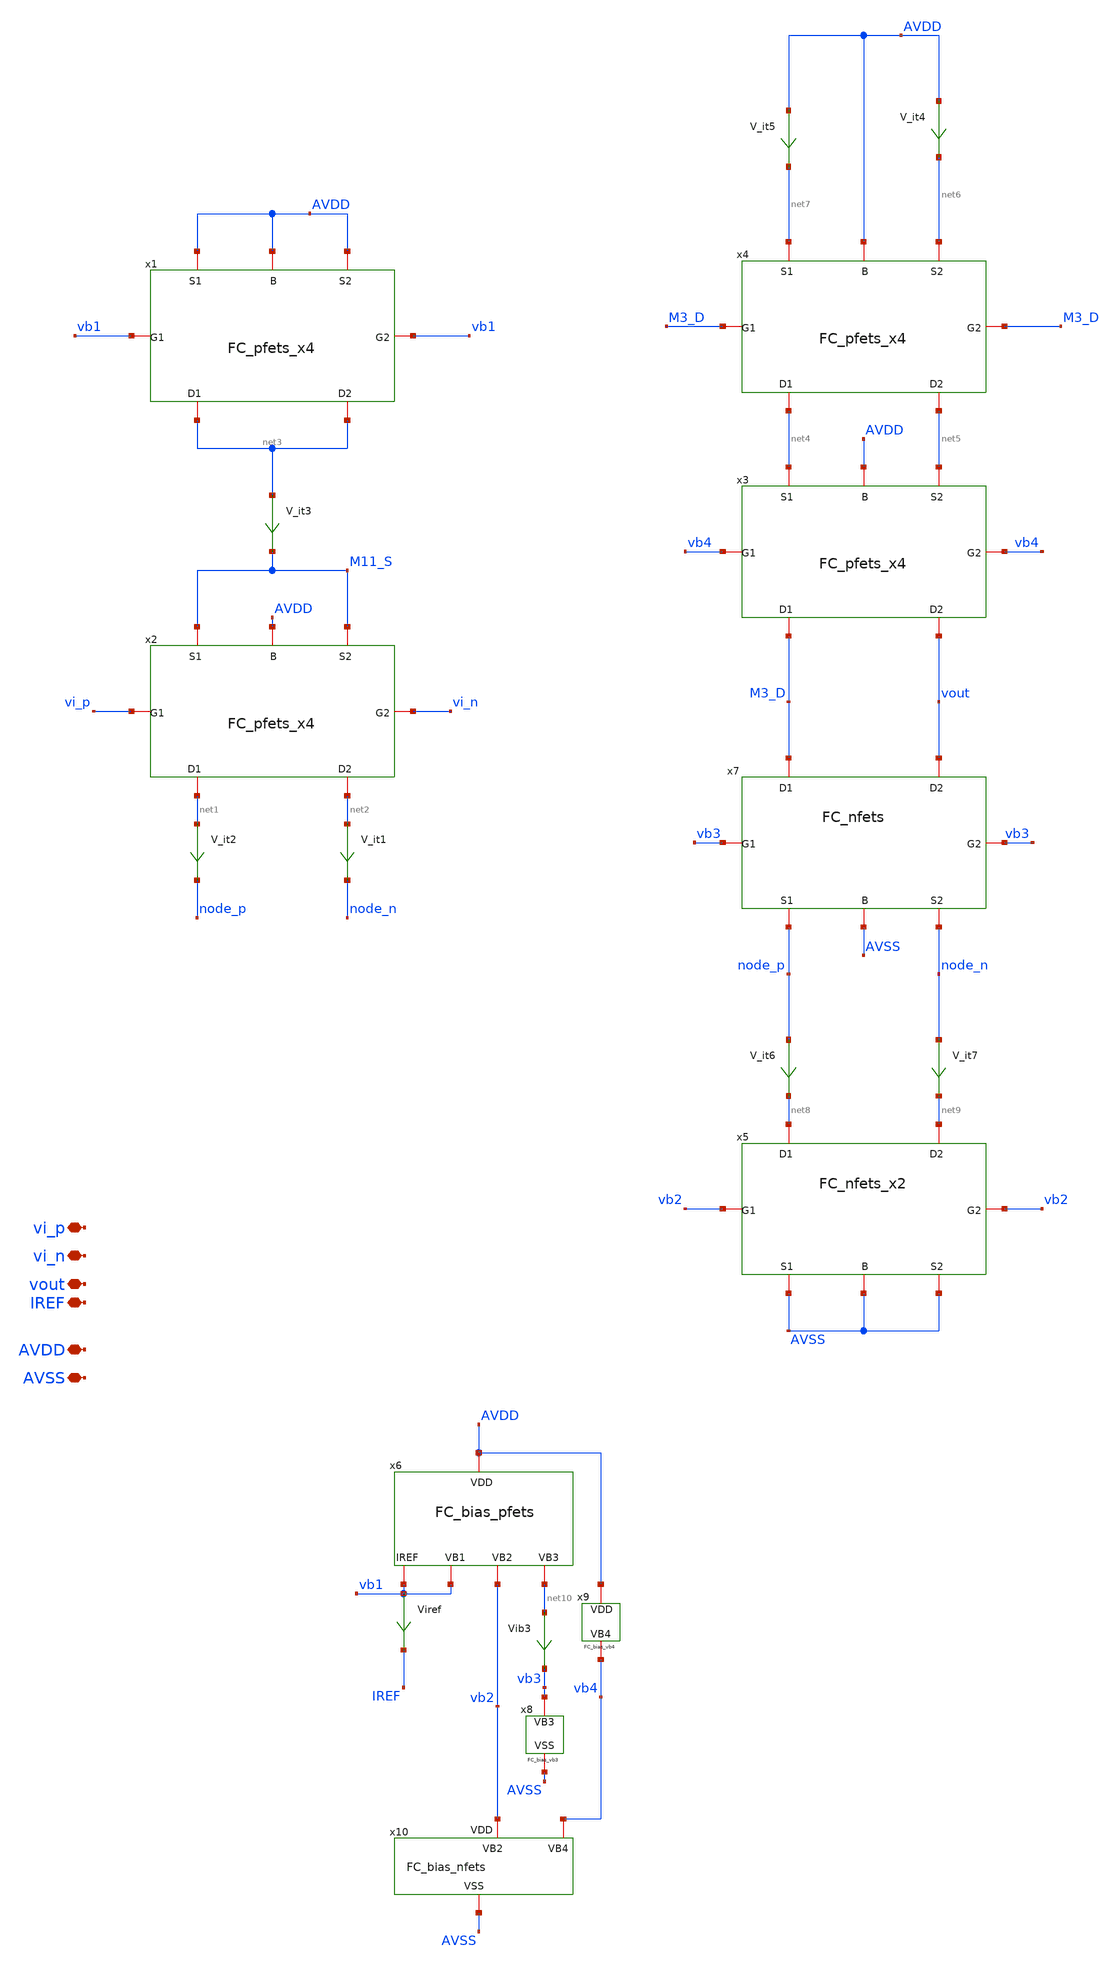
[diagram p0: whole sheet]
** sch_path: TIA_Filter/Folded/FoldedCascode.sch
**.subckt FoldedCascode AVDD AVSS vout vi_p vi_n IREF
*.iopin AVDD
*.iopin AVSS
*.iopin vout
*.iopin vi_p
*.iopin vi_n
*.iopin IREF
V_it1 net2 node_n 0
.save i(v_it1)
V_it2 net1 node_p 0
.save i(v_it2)
V_it3 net3 M11_S 0
.save i(v_it3)
V_it4 AVDD net6 0
.save i(v_it4)
V_it5 AVDD net7 0
.save i(v_it5)
V_it6 node_p net8 0
.save i(v_it6)
V_it7 node_n net9 0
.save i(v_it7)
x7 node_p node_n M3_D vout vb3 vb3 AVSS FC_nfets
x5 AVSS AVSS net8 net9 vb2 vb2 AVSS FC_nfets_x2
x1 AVDD AVDD net3 net3 vb1 vb1 AVDD FC_pfets_x4
x2 M11_S M11_S net1 net2 vi_p vi_n AVDD FC_pfets_x4
x3 net4 net5 M3_D vout vb4 vb4 AVDD FC_pfets_x4
x4 net7 net6 net4 net5 M3_D M3_D AVDD FC_pfets_x4
Viref vb1 IREF 0
.save i(viref)
Vib3 net10 vb3 0
.save i(vib3)
x6 vb1 vb2 net10 vb1 AVDD FC_bias_pfets
x8 vb3 AVSS FC_bias_vb3
x9 vb4 AVDD FC_bias_vb4
x10 vb2 vb4 AVSS FC_bias_nfets
**.ends
.end
